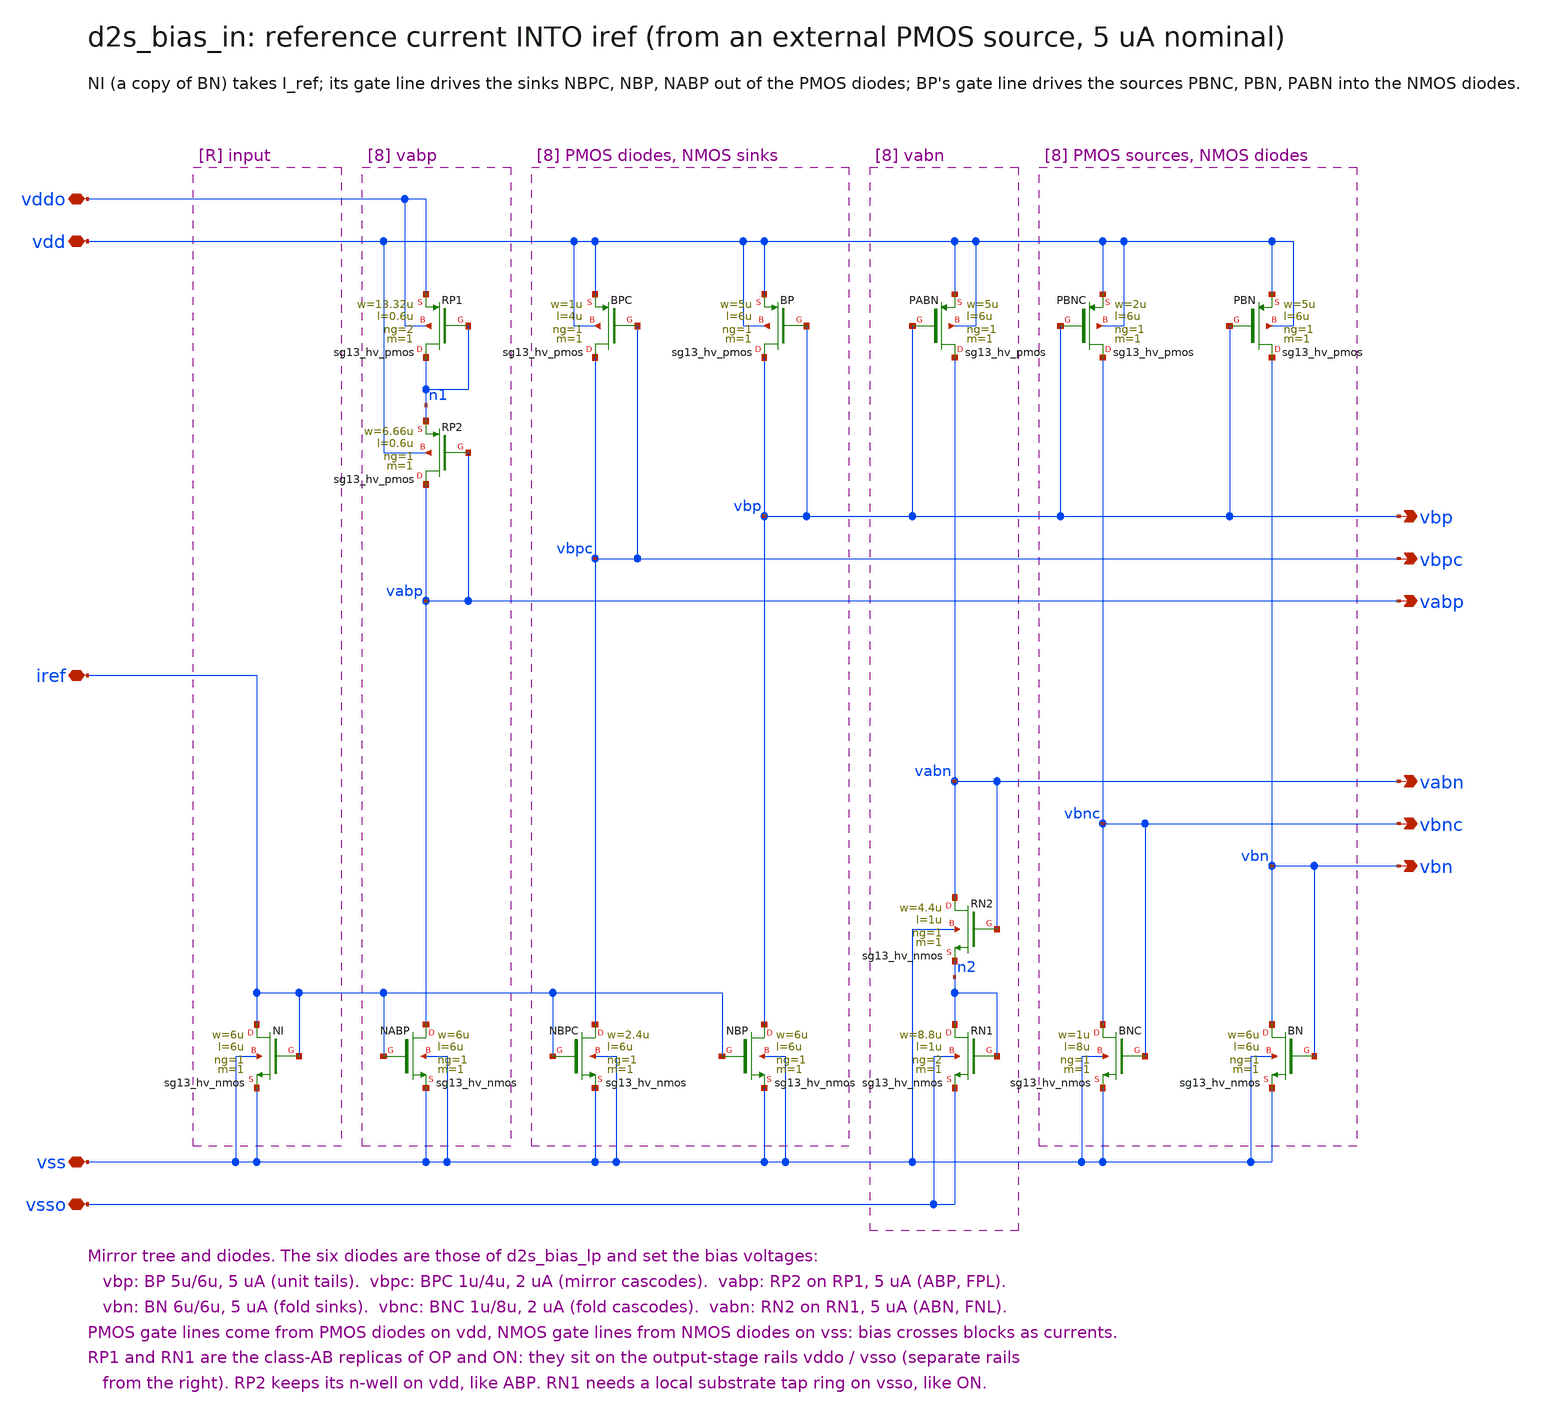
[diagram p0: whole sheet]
** sch_path: sudelbuecher/design_considerations/class_ab_pad_driver/improvements/xschem/d2s_bias_in.sch
**.subckt d2s_bias_in vdd vss vddo vsso iref vbp vbn vbpc vbnc vabp vabn
*.iopin vdd
*.iopin vss
*.iopin vddo
*.iopin vsso
*.iopin iref
*.opin vbp
*.opin vbn
*.opin vbpc
*.opin vbnc
*.opin vabp
*.opin vabn
XNI iref iref vss vss sg13_hv_nmos w=6u l=6u ng=1 m=1 mm_ok=1
XBPC vbpc vbpc vdd vdd sg13_hv_pmos w=1u l=4u ng=1 m=1 mm_ok=1
XNBPC vbpc iref vss vss sg13_hv_nmos w=2.4u l=6u ng=1 m=1 mm_ok=1
XBP vbp vbp vdd vdd sg13_hv_pmos w=5u l=6u ng=1 m=1 mm_ok=1
XNBP vbp iref vss vss sg13_hv_nmos w=6u l=6u ng=1 m=1 mm_ok=1
XRP1 n1 n1 vddo vddo sg13_hv_pmos w=13.32u l=0.6u ng=2 m=1 mm_ok=1
XRP2 vabp vabp n1 vdd sg13_hv_pmos w=6.66u l=0.6u ng=1 m=1 mm_ok=1
XNABP vabp iref vss vss sg13_hv_nmos w=6u l=6u ng=1 m=1 mm_ok=1
XPBNC vbnc vbp vdd vdd sg13_hv_pmos w=2u l=6u ng=1 m=1 mm_ok=1
XBNC vbnc vbnc vss vss sg13_hv_nmos w=1u l=8u ng=1 m=1 mm_ok=1
XPBN vbn vbp vdd vdd sg13_hv_pmos w=5u l=6u ng=1 m=1 mm_ok=1
XBN vbn vbn vss vss sg13_hv_nmos w=6u l=6u ng=1 m=1 mm_ok=1
XPABN vabn vbp vdd vdd sg13_hv_pmos w=5u l=6u ng=1 m=1 mm_ok=1
XRN2 vabn vabn n2 vss sg13_hv_nmos w=4.4u l=1u ng=1 m=1 mm_ok=1
XRN1 n2 n2 vsso vsso sg13_hv_nmos w=8.8u l=1u ng=2 m=1 mm_ok=1
**.ends
.end
